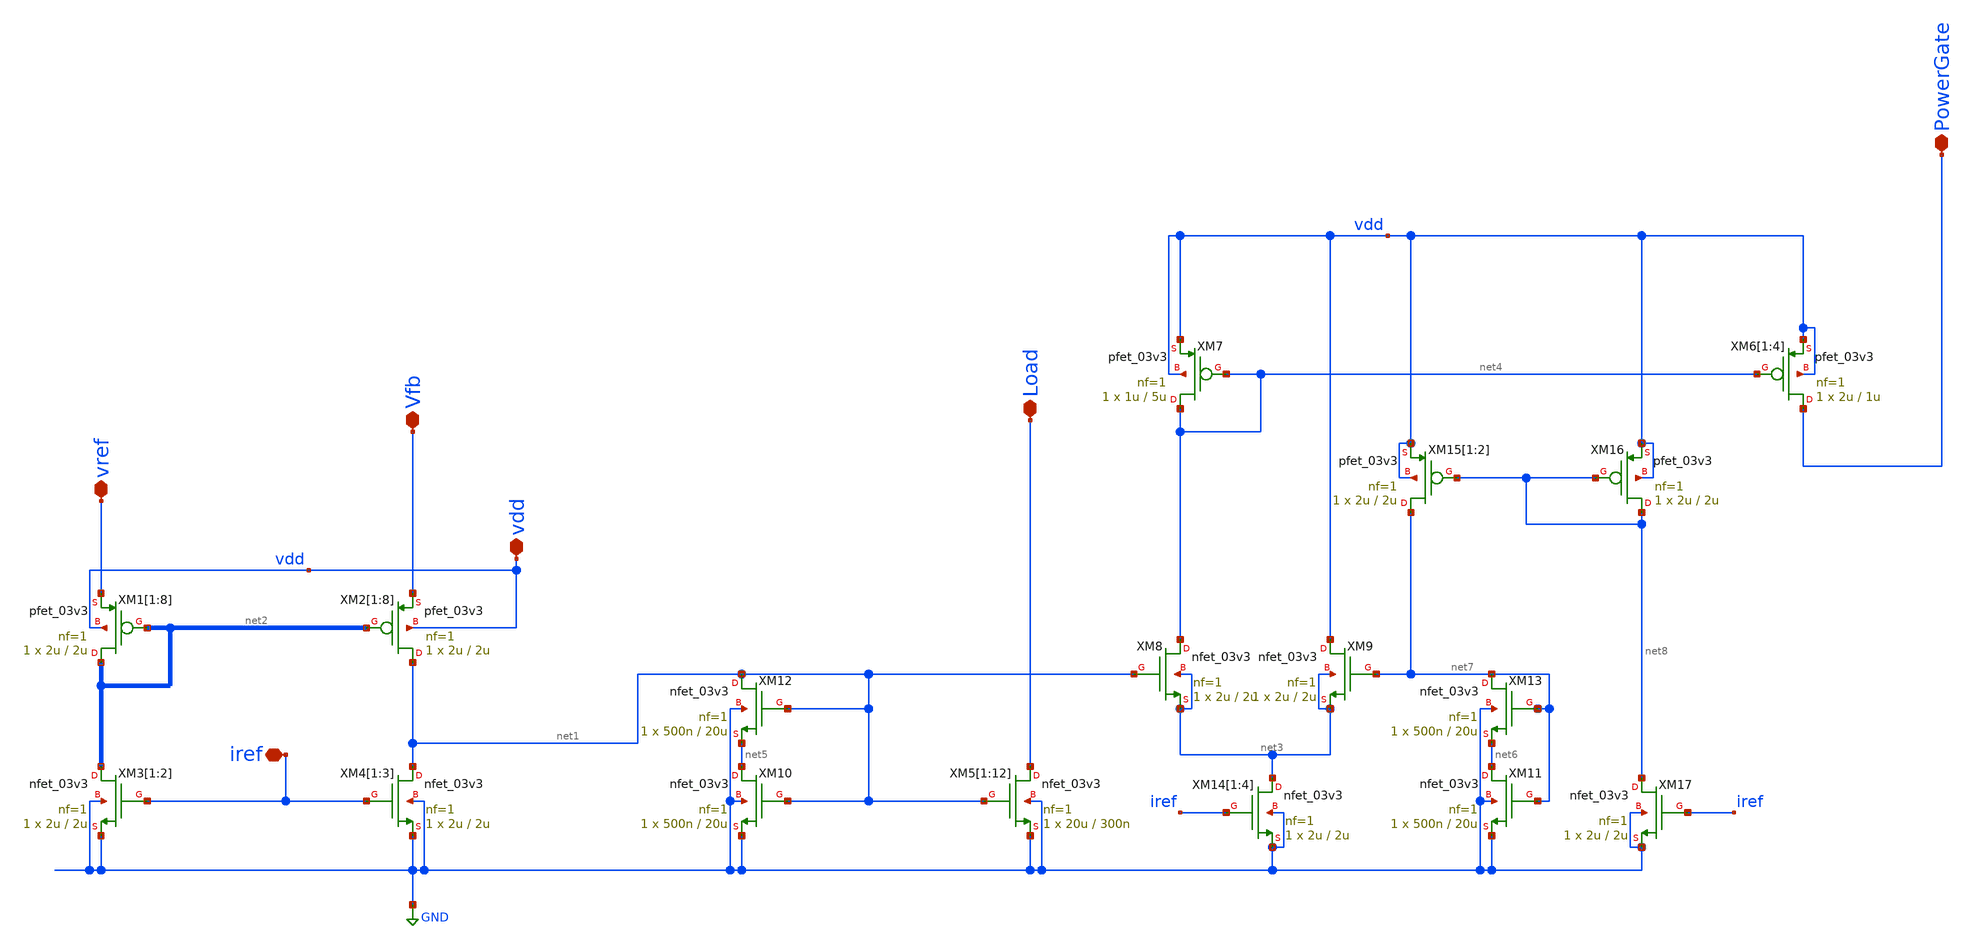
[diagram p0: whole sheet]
** sch_path: Voltage_Reference/LDO/overvoltageProtection.sch
**.subckt overvoltageProtection vref iref vdd Load Vfb PowerGate
*.iopin vref
*.iopin iref
*.iopin vdd
*.iopin Load
*.iopin Vfb
*.iopin PowerGate
XM2[1] net1 net2[1] Vfb vdd pfet_03v3 L=2u W=2u nf=1 ad='int((nf+1)/2) * W/nf * 0.18u' as='int((nf+2)/2) * W/nf * 0.18u'
+ pd='2*int((nf+1)/2) * (W/nf + 0.18u)' ps='2*int((nf+2)/2) * (W/nf + 0.18u)' nrd='0.18u / W' nrs='0.18u / W'
+ sa=0 sb=0 sd=0 m=1
XM2[2] net1 net2[0] Vfb vdd pfet_03v3 L=2u W=2u nf=1 ad='int((nf+1)/2) * W/nf * 0.18u' as='int((nf+2)/2) * W/nf * 0.18u'
+ pd='2*int((nf+1)/2) * (W/nf + 0.18u)' ps='2*int((nf+2)/2) * (W/nf + 0.18u)' nrd='0.18u / W' nrs='0.18u / W'
+ sa=0 sb=0 sd=0 m=1
XM2[3] net1 net2[1] Vfb vdd pfet_03v3 L=2u W=2u nf=1 ad='int((nf+1)/2) * W/nf * 0.18u' as='int((nf+2)/2) * W/nf * 0.18u'
+ pd='2*int((nf+1)/2) * (W/nf + 0.18u)' ps='2*int((nf+2)/2) * (W/nf + 0.18u)' nrd='0.18u / W' nrs='0.18u / W'
+ sa=0 sb=0 sd=0 m=1
XM2[4] net1 net2[0] Vfb vdd pfet_03v3 L=2u W=2u nf=1 ad='int((nf+1)/2) * W/nf * 0.18u' as='int((nf+2)/2) * W/nf * 0.18u'
+ pd='2*int((nf+1)/2) * (W/nf + 0.18u)' ps='2*int((nf+2)/2) * (W/nf + 0.18u)' nrd='0.18u / W' nrs='0.18u / W'
+ sa=0 sb=0 sd=0 m=1
XM2[5] net1 net2[1] Vfb vdd pfet_03v3 L=2u W=2u nf=1 ad='int((nf+1)/2) * W/nf * 0.18u' as='int((nf+2)/2) * W/nf * 0.18u'
+ pd='2*int((nf+1)/2) * (W/nf + 0.18u)' ps='2*int((nf+2)/2) * (W/nf + 0.18u)' nrd='0.18u / W' nrs='0.18u / W'
+ sa=0 sb=0 sd=0 m=1
XM2[6] net1 net2[0] Vfb vdd pfet_03v3 L=2u W=2u nf=1 ad='int((nf+1)/2) * W/nf * 0.18u' as='int((nf+2)/2) * W/nf * 0.18u'
+ pd='2*int((nf+1)/2) * (W/nf + 0.18u)' ps='2*int((nf+2)/2) * (W/nf + 0.18u)' nrd='0.18u / W' nrs='0.18u / W'
+ sa=0 sb=0 sd=0 m=1
XM2[7] net1 net2[1] Vfb vdd pfet_03v3 L=2u W=2u nf=1 ad='int((nf+1)/2) * W/nf * 0.18u' as='int((nf+2)/2) * W/nf * 0.18u'
+ pd='2*int((nf+1)/2) * (W/nf + 0.18u)' ps='2*int((nf+2)/2) * (W/nf + 0.18u)' nrd='0.18u / W' nrs='0.18u / W'
+ sa=0 sb=0 sd=0 m=1
XM2[8] net1 net2[0] Vfb vdd pfet_03v3 L=2u W=2u nf=1 ad='int((nf+1)/2) * W/nf * 0.18u' as='int((nf+2)/2) * W/nf * 0.18u'
+ pd='2*int((nf+1)/2) * (W/nf + 0.18u)' ps='2*int((nf+2)/2) * (W/nf + 0.18u)' nrd='0.18u / W' nrs='0.18u / W'
+ sa=0 sb=0 sd=0 m=1
XM4[1] net1 iref GND GND nfet_03v3 L=2u W=2u nf=1 ad='int((nf+1)/2) * W/nf * 0.18u' as='int((nf+2)/2) * W/nf * 0.18u'
+ pd='2*int((nf+1)/2) * (W/nf + 0.18u)' ps='2*int((nf+2)/2) * (W/nf + 0.18u)' nrd='0.18u / W' nrs='0.18u / W'
+ sa=0 sb=0 sd=0 m=1
XM4[2] net1 iref GND GND nfet_03v3 L=2u W=2u nf=1 ad='int((nf+1)/2) * W/nf * 0.18u' as='int((nf+2)/2) * W/nf * 0.18u'
+ pd='2*int((nf+1)/2) * (W/nf + 0.18u)' ps='2*int((nf+2)/2) * (W/nf + 0.18u)' nrd='0.18u / W' nrs='0.18u / W'
+ sa=0 sb=0 sd=0 m=1
XM4[3] net1 iref GND GND nfet_03v3 L=2u W=2u nf=1 ad='int((nf+1)/2) * W/nf * 0.18u' as='int((nf+2)/2) * W/nf * 0.18u'
+ pd='2*int((nf+1)/2) * (W/nf + 0.18u)' ps='2*int((nf+2)/2) * (W/nf + 0.18u)' nrd='0.18u / W' nrs='0.18u / W'
+ sa=0 sb=0 sd=0 m=1
XM5[1] Load net1 GND GND nfet_03v3 L=300n W=20u nf=1 ad='int((nf+1)/2) * W/nf * 0.18u' as='int((nf+2)/2) * W/nf * 0.18u'
+ pd='2*int((nf+1)/2) * (W/nf + 0.18u)' ps='2*int((nf+2)/2) * (W/nf + 0.18u)' nrd='0.18u / W' nrs='0.18u / W'
+ sa=0 sb=0 sd=0 m=1
XM5[2] Load net1 GND GND nfet_03v3 L=300n W=20u nf=1 ad='int((nf+1)/2) * W/nf * 0.18u' as='int((nf+2)/2) * W/nf * 0.18u'
+ pd='2*int((nf+1)/2) * (W/nf + 0.18u)' ps='2*int((nf+2)/2) * (W/nf + 0.18u)' nrd='0.18u / W' nrs='0.18u / W'
+ sa=0 sb=0 sd=0 m=1
XM5[3] Load net1 GND GND nfet_03v3 L=300n W=20u nf=1 ad='int((nf+1)/2) * W/nf * 0.18u' as='int((nf+2)/2) * W/nf * 0.18u'
+ pd='2*int((nf+1)/2) * (W/nf + 0.18u)' ps='2*int((nf+2)/2) * (W/nf + 0.18u)' nrd='0.18u / W' nrs='0.18u / W'
+ sa=0 sb=0 sd=0 m=1
XM5[4] Load net1 GND GND nfet_03v3 L=300n W=20u nf=1 ad='int((nf+1)/2) * W/nf * 0.18u' as='int((nf+2)/2) * W/nf * 0.18u'
+ pd='2*int((nf+1)/2) * (W/nf + 0.18u)' ps='2*int((nf+2)/2) * (W/nf + 0.18u)' nrd='0.18u / W' nrs='0.18u / W'
+ sa=0 sb=0 sd=0 m=1
XM5[5] Load net1 GND GND nfet_03v3 L=300n W=20u nf=1 ad='int((nf+1)/2) * W/nf * 0.18u' as='int((nf+2)/2) * W/nf * 0.18u'
+ pd='2*int((nf+1)/2) * (W/nf + 0.18u)' ps='2*int((nf+2)/2) * (W/nf + 0.18u)' nrd='0.18u / W' nrs='0.18u / W'
+ sa=0 sb=0 sd=0 m=1
XM5[6] Load net1 GND GND nfet_03v3 L=300n W=20u nf=1 ad='int((nf+1)/2) * W/nf * 0.18u' as='int((nf+2)/2) * W/nf * 0.18u'
+ pd='2*int((nf+1)/2) * (W/nf + 0.18u)' ps='2*int((nf+2)/2) * (W/nf + 0.18u)' nrd='0.18u / W' nrs='0.18u / W'
+ sa=0 sb=0 sd=0 m=1
XM5[7] Load net1 GND GND nfet_03v3 L=300n W=20u nf=1 ad='int((nf+1)/2) * W/nf * 0.18u' as='int((nf+2)/2) * W/nf * 0.18u'
+ pd='2*int((nf+1)/2) * (W/nf + 0.18u)' ps='2*int((nf+2)/2) * (W/nf + 0.18u)' nrd='0.18u / W' nrs='0.18u / W'
+ sa=0 sb=0 sd=0 m=1
XM5[8] Load net1 GND GND nfet_03v3 L=300n W=20u nf=1 ad='int((nf+1)/2) * W/nf * 0.18u' as='int((nf+2)/2) * W/nf * 0.18u'
+ pd='2*int((nf+1)/2) * (W/nf + 0.18u)' ps='2*int((nf+2)/2) * (W/nf + 0.18u)' nrd='0.18u / W' nrs='0.18u / W'
+ sa=0 sb=0 sd=0 m=1
XM5[9] Load net1 GND GND nfet_03v3 L=300n W=20u nf=1 ad='int((nf+1)/2) * W/nf * 0.18u' as='int((nf+2)/2) * W/nf * 0.18u'
+ pd='2*int((nf+1)/2) * (W/nf + 0.18u)' ps='2*int((nf+2)/2) * (W/nf + 0.18u)' nrd='0.18u / W' nrs='0.18u / W'
+ sa=0 sb=0 sd=0 m=1
XM5[10] Load net1 GND GND nfet_03v3 L=300n W=20u nf=1 ad='int((nf+1)/2) * W/nf * 0.18u' as='int((nf+2)/2) * W/nf * 0.18u'
+ pd='2*int((nf+1)/2) * (W/nf + 0.18u)' ps='2*int((nf+2)/2) * (W/nf + 0.18u)' nrd='0.18u / W' nrs='0.18u / W'
+ sa=0 sb=0 sd=0 m=1
XM5[11] Load net1 GND GND nfet_03v3 L=300n W=20u nf=1 ad='int((nf+1)/2) * W/nf * 0.18u' as='int((nf+2)/2) * W/nf * 0.18u'
+ pd='2*int((nf+1)/2) * (W/nf + 0.18u)' ps='2*int((nf+2)/2) * (W/nf + 0.18u)' nrd='0.18u / W' nrs='0.18u / W'
+ sa=0 sb=0 sd=0 m=1
XM5[12] Load net1 GND GND nfet_03v3 L=300n W=20u nf=1 ad='int((nf+1)/2) * W/nf * 0.18u' as='int((nf+2)/2) * W/nf * 0.18u'
+ pd='2*int((nf+1)/2) * (W/nf + 0.18u)' ps='2*int((nf+2)/2) * (W/nf + 0.18u)' nrd='0.18u / W' nrs='0.18u / W'
+ sa=0 sb=0 sd=0 m=1
XM1[1] net2[1] net2[1] vref vdd pfet_03v3 L=2u W=2u nf=1 ad='int((nf+1)/2) * W/nf * 0.18u' as='int((nf+2)/2) * W/nf * 0.18u'
+ pd='2*int((nf+1)/2) * (W/nf + 0.18u)' ps='2*int((nf+2)/2) * (W/nf + 0.18u)' nrd='0.18u / W' nrs='0.18u / W'
+ sa=0 sb=0 sd=0 m=1
XM1[2] net2[0] net2[0] vref vdd pfet_03v3 L=2u W=2u nf=1 ad='int((nf+1)/2) * W/nf * 0.18u' as='int((nf+2)/2) * W/nf * 0.18u'
+ pd='2*int((nf+1)/2) * (W/nf + 0.18u)' ps='2*int((nf+2)/2) * (W/nf + 0.18u)' nrd='0.18u / W' nrs='0.18u / W'
+ sa=0 sb=0 sd=0 m=1
XM1[3] net2[1] net2[1] vref vdd pfet_03v3 L=2u W=2u nf=1 ad='int((nf+1)/2) * W/nf * 0.18u' as='int((nf+2)/2) * W/nf * 0.18u'
+ pd='2*int((nf+1)/2) * (W/nf + 0.18u)' ps='2*int((nf+2)/2) * (W/nf + 0.18u)' nrd='0.18u / W' nrs='0.18u / W'
+ sa=0 sb=0 sd=0 m=1
XM1[4] net2[0] net2[0] vref vdd pfet_03v3 L=2u W=2u nf=1 ad='int((nf+1)/2) * W/nf * 0.18u' as='int((nf+2)/2) * W/nf * 0.18u'
+ pd='2*int((nf+1)/2) * (W/nf + 0.18u)' ps='2*int((nf+2)/2) * (W/nf + 0.18u)' nrd='0.18u / W' nrs='0.18u / W'
+ sa=0 sb=0 sd=0 m=1
XM1[5] net2[1] net2[1] vref vdd pfet_03v3 L=2u W=2u nf=1 ad='int((nf+1)/2) * W/nf * 0.18u' as='int((nf+2)/2) * W/nf * 0.18u'
+ pd='2*int((nf+1)/2) * (W/nf + 0.18u)' ps='2*int((nf+2)/2) * (W/nf + 0.18u)' nrd='0.18u / W' nrs='0.18u / W'
+ sa=0 sb=0 sd=0 m=1
XM1[6] net2[0] net2[0] vref vdd pfet_03v3 L=2u W=2u nf=1 ad='int((nf+1)/2) * W/nf * 0.18u' as='int((nf+2)/2) * W/nf * 0.18u'
+ pd='2*int((nf+1)/2) * (W/nf + 0.18u)' ps='2*int((nf+2)/2) * (W/nf + 0.18u)' nrd='0.18u / W' nrs='0.18u / W'
+ sa=0 sb=0 sd=0 m=1
XM1[7] net2[1] net2[1] vref vdd pfet_03v3 L=2u W=2u nf=1 ad='int((nf+1)/2) * W/nf * 0.18u' as='int((nf+2)/2) * W/nf * 0.18u'
+ pd='2*int((nf+1)/2) * (W/nf + 0.18u)' ps='2*int((nf+2)/2) * (W/nf + 0.18u)' nrd='0.18u / W' nrs='0.18u / W'
+ sa=0 sb=0 sd=0 m=1
XM1[8] net2[0] net2[0] vref vdd pfet_03v3 L=2u W=2u nf=1 ad='int((nf+1)/2) * W/nf * 0.18u' as='int((nf+2)/2) * W/nf * 0.18u'
+ pd='2*int((nf+1)/2) * (W/nf + 0.18u)' ps='2*int((nf+2)/2) * (W/nf + 0.18u)' nrd='0.18u / W' nrs='0.18u / W'
+ sa=0 sb=0 sd=0 m=1
XM3[1] net2[1] iref GND GND nfet_03v3 L=2u W=2u nf=1 ad='int((nf+1)/2) * W/nf * 0.18u' as='int((nf+2)/2) * W/nf * 0.18u'
+ pd='2*int((nf+1)/2) * (W/nf + 0.18u)' ps='2*int((nf+2)/2) * (W/nf + 0.18u)' nrd='0.18u / W' nrs='0.18u / W'
+ sa=0 sb=0 sd=0 m=1
XM3[2] net2[0] iref GND GND nfet_03v3 L=2u W=2u nf=1 ad='int((nf+1)/2) * W/nf * 0.18u' as='int((nf+2)/2) * W/nf * 0.18u'
+ pd='2*int((nf+1)/2) * (W/nf + 0.18u)' ps='2*int((nf+2)/2) * (W/nf + 0.18u)' nrd='0.18u / W' nrs='0.18u / W'
+ sa=0 sb=0 sd=0 m=1
XM6[1] PowerGate net4 vdd vdd pfet_03v3 L=1u W=2u nf=1 ad='int((nf+1)/2) * W/nf * 0.18u' as='int((nf+2)/2) * W/nf * 0.18u'
+ pd='2*int((nf+1)/2) * (W/nf + 0.18u)' ps='2*int((nf+2)/2) * (W/nf + 0.18u)' nrd='0.18u / W' nrs='0.18u / W'
+ sa=0 sb=0 sd=0 m=1
XM6[2] PowerGate net4 vdd vdd pfet_03v3 L=1u W=2u nf=1 ad='int((nf+1)/2) * W/nf * 0.18u' as='int((nf+2)/2) * W/nf * 0.18u'
+ pd='2*int((nf+1)/2) * (W/nf + 0.18u)' ps='2*int((nf+2)/2) * (W/nf + 0.18u)' nrd='0.18u / W' nrs='0.18u / W'
+ sa=0 sb=0 sd=0 m=1
XM6[3] PowerGate net4 vdd vdd pfet_03v3 L=1u W=2u nf=1 ad='int((nf+1)/2) * W/nf * 0.18u' as='int((nf+2)/2) * W/nf * 0.18u'
+ pd='2*int((nf+1)/2) * (W/nf + 0.18u)' ps='2*int((nf+2)/2) * (W/nf + 0.18u)' nrd='0.18u / W' nrs='0.18u / W'
+ sa=0 sb=0 sd=0 m=1
XM6[4] PowerGate net4 vdd vdd pfet_03v3 L=1u W=2u nf=1 ad='int((nf+1)/2) * W/nf * 0.18u' as='int((nf+2)/2) * W/nf * 0.18u'
+ pd='2*int((nf+1)/2) * (W/nf + 0.18u)' ps='2*int((nf+2)/2) * (W/nf + 0.18u)' nrd='0.18u / W' nrs='0.18u / W'
+ sa=0 sb=0 sd=0 m=1
XM7 net4 net4 vdd vdd pfet_03v3 L=5u W=1u nf=1 ad='int((nf+1)/2) * W/nf * 0.18u' as='int((nf+2)/2) * W/nf * 0.18u'
+ pd='2*int((nf+1)/2) * (W/nf + 0.18u)' ps='2*int((nf+2)/2) * (W/nf + 0.18u)' nrd='0.18u / W' nrs='0.18u / W'
+ sa=0 sb=0 sd=0 m=1
XM8 net4 net1 net3 net3 nfet_03v3 L=2u W=2u nf=1 ad='int((nf+1)/2) * W/nf * 0.18u' as='int((nf+2)/2) * W/nf * 0.18u'
+ pd='2*int((nf+1)/2) * (W/nf + 0.18u)' ps='2*int((nf+2)/2) * (W/nf + 0.18u)' nrd='0.18u / W' nrs='0.18u / W'
+ sa=0 sb=0 sd=0 m=1
XM10 net5 net1 GND GND nfet_03v3 L=20u W=500n nf=1 ad='int((nf+1)/2) * W/nf * 0.18u' as='int((nf+2)/2) * W/nf * 0.18u'
+ pd='2*int((nf+1)/2) * (W/nf + 0.18u)' ps='2*int((nf+2)/2) * (W/nf + 0.18u)' nrd='0.18u / W' nrs='0.18u / W'
+ sa=0 sb=0 sd=0 m=1
XM12 net1 net1 net5 GND nfet_03v3 L=20u W=500n nf=1 ad='int((nf+1)/2) * W/nf * 0.18u' as='int((nf+2)/2) * W/nf * 0.18u'
+ pd='2*int((nf+1)/2) * (W/nf + 0.18u)' ps='2*int((nf+2)/2) * (W/nf + 0.18u)' nrd='0.18u / W' nrs='0.18u / W'
+ sa=0 sb=0 sd=0 m=1
XM9 vdd net7 net3 net3 nfet_03v3 L=2u W=2u nf=1 ad='int((nf+1)/2) * W/nf * 0.18u' as='int((nf+2)/2) * W/nf * 0.18u'
+ pd='2*int((nf+1)/2) * (W/nf + 0.18u)' ps='2*int((nf+2)/2) * (W/nf + 0.18u)' nrd='0.18u / W' nrs='0.18u / W'
+ sa=0 sb=0 sd=0 m=1
XM11 net6 net7 GND GND nfet_03v3 L=20u W=500n nf=1 ad='int((nf+1)/2) * W/nf * 0.18u' as='int((nf+2)/2) * W/nf * 0.18u'
+ pd='2*int((nf+1)/2) * (W/nf + 0.18u)' ps='2*int((nf+2)/2) * (W/nf + 0.18u)' nrd='0.18u / W' nrs='0.18u / W'
+ sa=0 sb=0 sd=0 m=1
XM13 net7 net7 net6 GND nfet_03v3 L=20u W=500n nf=1 ad='int((nf+1)/2) * W/nf * 0.18u' as='int((nf+2)/2) * W/nf * 0.18u'
+ pd='2*int((nf+1)/2) * (W/nf + 0.18u)' ps='2*int((nf+2)/2) * (W/nf + 0.18u)' nrd='0.18u / W' nrs='0.18u / W'
+ sa=0 sb=0 sd=0 m=1
XM14[1] net3 iref GND GND nfet_03v3 L=2u W=2u nf=1 ad='int((nf+1)/2) * W/nf * 0.18u' as='int((nf+2)/2) * W/nf * 0.18u'
+ pd='2*int((nf+1)/2) * (W/nf + 0.18u)' ps='2*int((nf+2)/2) * (W/nf + 0.18u)' nrd='0.18u / W' nrs='0.18u / W'
+ sa=0 sb=0 sd=0 m=1
XM14[2] net3 iref GND GND nfet_03v3 L=2u W=2u nf=1 ad='int((nf+1)/2) * W/nf * 0.18u' as='int((nf+2)/2) * W/nf * 0.18u'
+ pd='2*int((nf+1)/2) * (W/nf + 0.18u)' ps='2*int((nf+2)/2) * (W/nf + 0.18u)' nrd='0.18u / W' nrs='0.18u / W'
+ sa=0 sb=0 sd=0 m=1
XM14[3] net3 iref GND GND nfet_03v3 L=2u W=2u nf=1 ad='int((nf+1)/2) * W/nf * 0.18u' as='int((nf+2)/2) * W/nf * 0.18u'
+ pd='2*int((nf+1)/2) * (W/nf + 0.18u)' ps='2*int((nf+2)/2) * (W/nf + 0.18u)' nrd='0.18u / W' nrs='0.18u / W'
+ sa=0 sb=0 sd=0 m=1
XM14[4] net3 iref GND GND nfet_03v3 L=2u W=2u nf=1 ad='int((nf+1)/2) * W/nf * 0.18u' as='int((nf+2)/2) * W/nf * 0.18u'
+ pd='2*int((nf+1)/2) * (W/nf + 0.18u)' ps='2*int((nf+2)/2) * (W/nf + 0.18u)' nrd='0.18u / W' nrs='0.18u / W'
+ sa=0 sb=0 sd=0 m=1
XM15[1] net7 net8 vdd vdd pfet_03v3 L=2u W=2u nf=1 ad='int((nf+1)/2) * W/nf * 0.18u' as='int((nf+2)/2) * W/nf * 0.18u'
+ pd='2*int((nf+1)/2) * (W/nf + 0.18u)' ps='2*int((nf+2)/2) * (W/nf + 0.18u)' nrd='0.18u / W' nrs='0.18u / W'
+ sa=0 sb=0 sd=0 m=1
XM15[2] net7 net8 vdd vdd pfet_03v3 L=2u W=2u nf=1 ad='int((nf+1)/2) * W/nf * 0.18u' as='int((nf+2)/2) * W/nf * 0.18u'
+ pd='2*int((nf+1)/2) * (W/nf + 0.18u)' ps='2*int((nf+2)/2) * (W/nf + 0.18u)' nrd='0.18u / W' nrs='0.18u / W'
+ sa=0 sb=0 sd=0 m=1
XM16 net8 net8 vdd vdd pfet_03v3 L=2u W=2u nf=1 ad='int((nf+1)/2) * W/nf * 0.18u' as='int((nf+2)/2) * W/nf * 0.18u'
+ pd='2*int((nf+1)/2) * (W/nf + 0.18u)' ps='2*int((nf+2)/2) * (W/nf + 0.18u)' nrd='0.18u / W' nrs='0.18u / W'
+ sa=0 sb=0 sd=0 m=1
XM17 net8 iref GND GND nfet_03v3 L=2u W=2u nf=1 ad='int((nf+1)/2) * W/nf * 0.18u' as='int((nf+2)/2) * W/nf * 0.18u'
+ pd='2*int((nf+1)/2) * (W/nf + 0.18u)' ps='2*int((nf+2)/2) * (W/nf + 0.18u)' nrd='0.18u / W' nrs='0.18u / W'
+ sa=0 sb=0 sd=0 m=1
**.ends
.GLOBAL GND
.end
